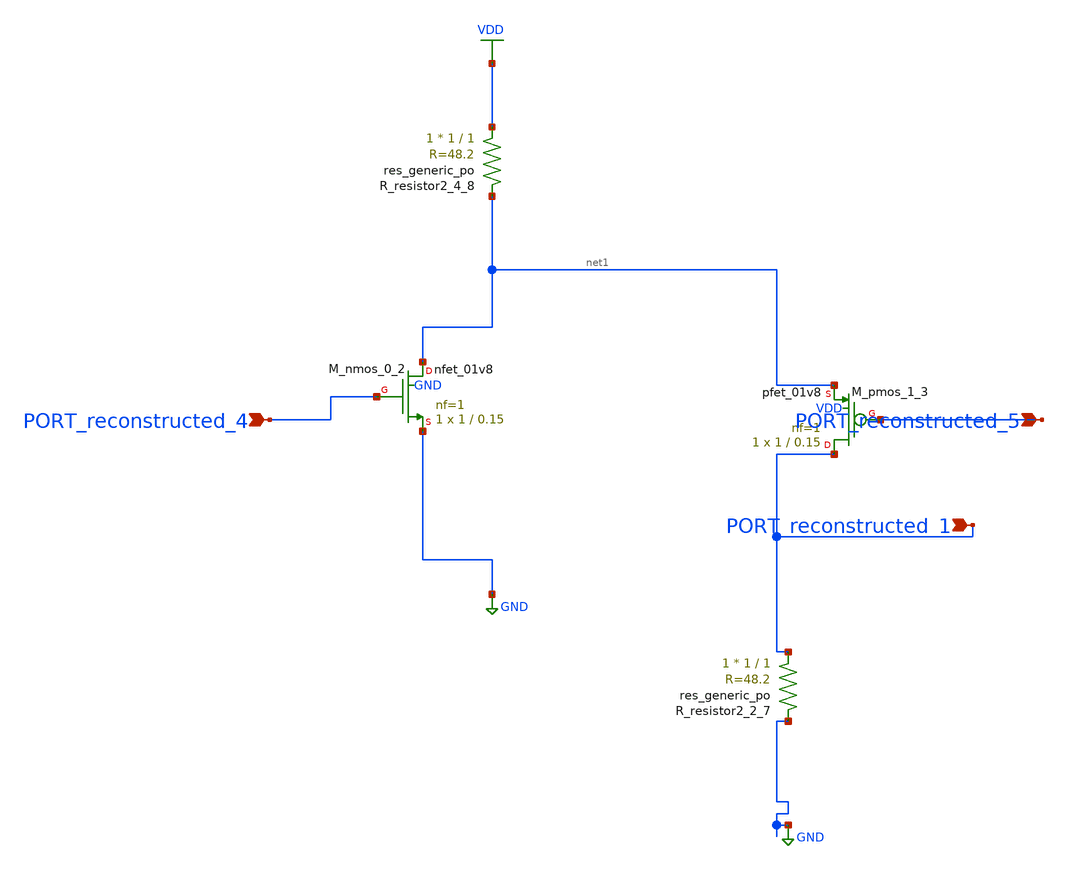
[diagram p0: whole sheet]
** sch_path: schematics/AMSNet/511.sch
**.subckt 511 PORT_reconstructed_5 PORT_reconstructed_4 PORT_reconstructed_1
*.ipin PORT_reconstructed_5
*.ipin PORT_reconstructed_4
*.ipin PORT_reconstructed_1
XM_nmos_0_2 net1 PORT_reconstructed_4 GND GND sky130_fd_pr__nfet_01v8 L=0.15 W=1 nf=1 ad='int((1 + 1)/2) * 1 / 1 * 0.29'
+ as='int((1 + 2)/2) * 1 / 1 * 0.29' pd='2*int((1 + 1)/2) * (1 / 1 + 0.29)' ps='2*int((1 + 2)/2) * (1 / 1 + 0.29)'
+ nrd='0.29 / 1 ' nrs='0.29 / 1 ' sa=0 sb=0 sd=0 mult=1 m=1
XM_pmos_1_3 PORT_reconstructed_1 PORT_reconstructed_5 net1 VDD sky130_fd_pr__pfet_01v8 L=0.15 W=1 nf=1
+ ad='int((1 + 1)/2) * 1 / 1 * 0.29' as='int((1 + 2)/2) * 1 / 1 * 0.29' pd='2*int((1 + 1)/2) * (1 / 1 + 0.29)'
+ ps='2*int((1 + 2)/2) * (1 / 1 + 0.29)' nrd='0.29 / 1 ' nrs='0.29 / 1 ' sa=0 sb=0 sd=0 mult=1 m=1
XR_resistor2_2_7 PORT_reconstructed_1 GND sky130_fd_pr__res_generic_po W=1 L=1 m=1
XR_resistor2_4_8 VDD net1 sky130_fd_pr__res_generic_po W=1 L=1 m=1
**.ends
.GLOBAL GND
.GLOBAL VDD
.end
